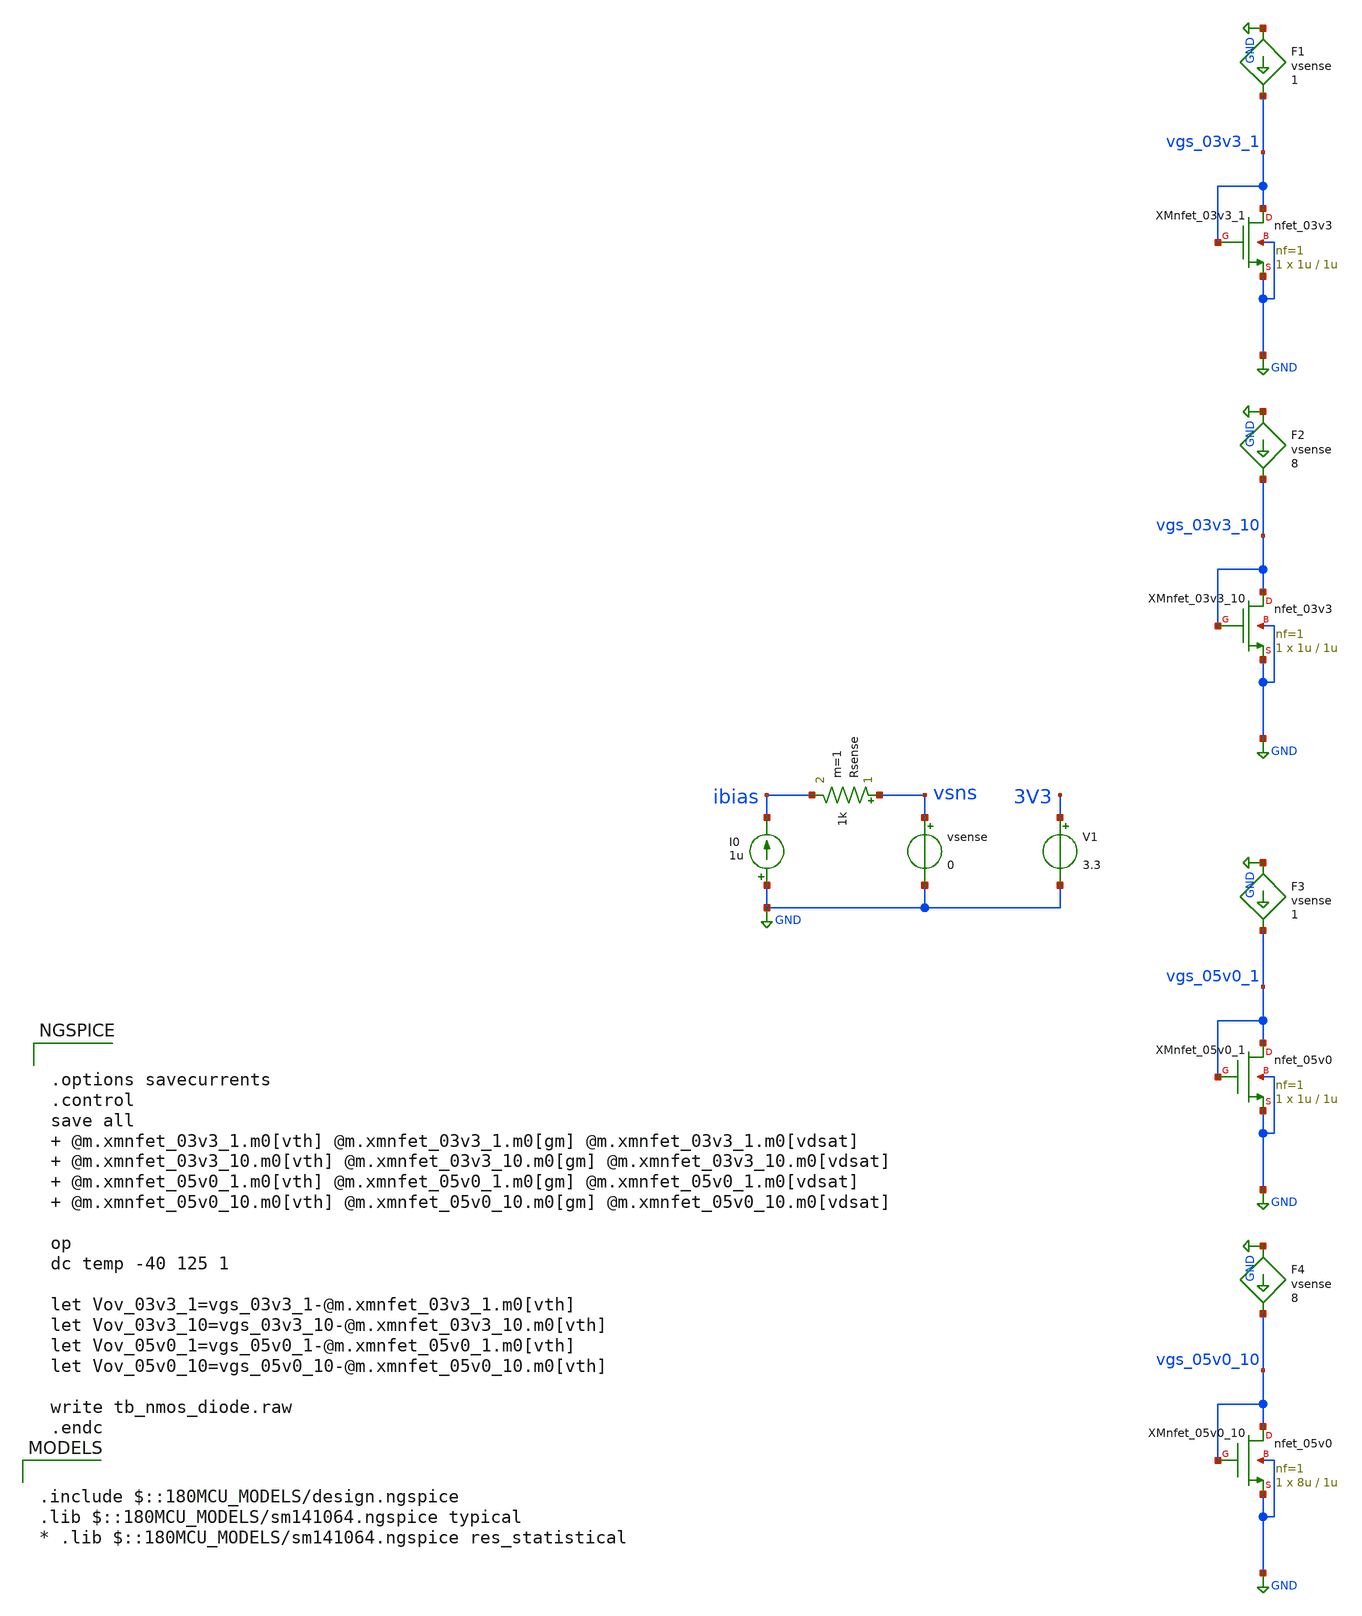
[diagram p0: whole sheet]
** sch_path: designs/libs/tb_analog/tb_nmos_diode/tb_nmos_diode.sch
**.subckt tb_nmos_diode
I0 GND ibias 1u
Rsense vsns ibias 1k m=1
vsense vsns GND 0
V1 3V3 GND 3.3
F1 GND vgs_03v3_1 vsense 1
F2 GND vgs_03v3_10 vsense 8
XMnfet_03v3_1 vgs_03v3_1 vgs_03v3_1 GND GND nfet_03v3 L=1u W=1u nf=1 ad='int((nf+1)/2) * W/nf * 0.18u'
+ as='int((nf+2)/2) * W/nf * 0.18u' pd='2*int((nf+1)/2) * (W/nf + 0.18u)' ps='2*int((nf+2)/2) * (W/nf + 0.18u)'
+ nrd='0.18u / W' nrs='0.18u / W' sa=0 sb=0 sd=0 m=1
XMnfet_03v3_10 vgs_03v3_10 vgs_03v3_10 GND GND nfet_03v3 L=1u W=1u nf=1 ad='int((nf+1)/2) * W/nf * 0.18u'
+ as='int((nf+2)/2) * W/nf * 0.18u' pd='2*int((nf+1)/2) * (W/nf + 0.18u)' ps='2*int((nf+2)/2) * (W/nf + 0.18u)'
+ nrd='0.18u / W' nrs='0.18u / W' sa=0 sb=0 sd=0 m=1
F3 GND vgs_05v0_1 vsense 1
F4 GND vgs_05v0_10 vsense 8
XMnfet_05v0_1 vgs_05v0_1 vgs_05v0_1 GND GND nfet_05v0 L=1u W=1u nf=1 ad='int((nf+1)/2) * W/nf * 0.18u'
+ as='int((nf+2)/2) * W/nf * 0.18u' pd='2*int((nf+1)/2) * (W/nf + 0.18u)' ps='2*int((nf+2)/2) * (W/nf + 0.18u)'
+ nrd='0.18u / W' nrs='0.18u / W' sa=0 sb=0 sd=0 m=1
XMnfet_05v0_10 vgs_05v0_10 vgs_05v0_10 GND GND nfet_05v0 L=1u W=8u nf=1 ad='int((nf+1)/2) * W/nf * 0.18u'
+ as='int((nf+2)/2) * W/nf * 0.18u' pd='2*int((nf+1)/2) * (W/nf + 0.18u)' ps='2*int((nf+2)/2) * (W/nf + 0.18u)'
+ nrd='0.18u / W' nrs='0.18u / W' sa=0 sb=0 sd=0 m=1
**** begin user architecture code

.include $::180MCU_MODELS/design.ngspice
.lib $::180MCU_MODELS/sm141064.ngspice typical
* .lib $::180MCU_MODELS/sm141064.ngspice res_statistical



.options savecurrents
.control
save all   @m.xmnfet_03v3_1.m0[vth] @m.xmnfet_03v3_1.m0[gm] @m.xmnfet_03v3_1.m0[vdsat]
+  @m.xmnfet_03v3_10.m0[vth] @m.xmnfet_03v3_10.m0[gm] @m.xmnfet_03v3_10.m0[vdsat]  @m.xmnfet_05v0_1.m0[vth]
+ @m.xmnfet_05v0_1.m0[gm] @m.xmnfet_05v0_1.m0[vdsat]  @m.xmnfet_05v0_10.m0[vth] @m.xmnfet_05v0_10.m0[gm]
+ @m.xmnfet_05v0_10.m0[vdsat]

op
dc temp -40 125 1

let Vov_03v3_1=vgs_03v3_1-@m.xmnfet_03v3_1.m0[vth]
let Vov_03v3_10=vgs_03v3_10-@m.xmnfet_03v3_10.m0[vth]
let Vov_05v0_1=vgs_05v0_1-@m.xmnfet_05v0_1.m0[vth]
let Vov_05v0_10=vgs_05v0_10-@m.xmnfet_05v0_10.m0[vth]

write tb_nmos_diode.raw
.endc


**** end user architecture code
**.ends
.GLOBAL GND
.end
